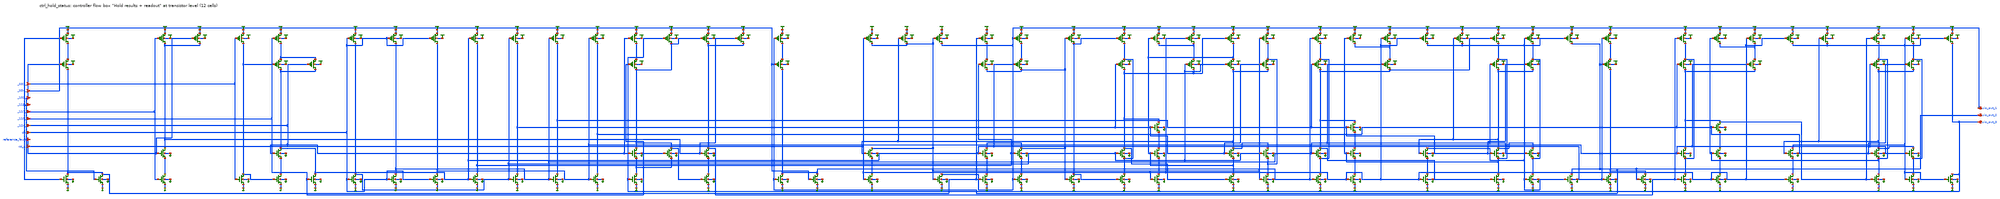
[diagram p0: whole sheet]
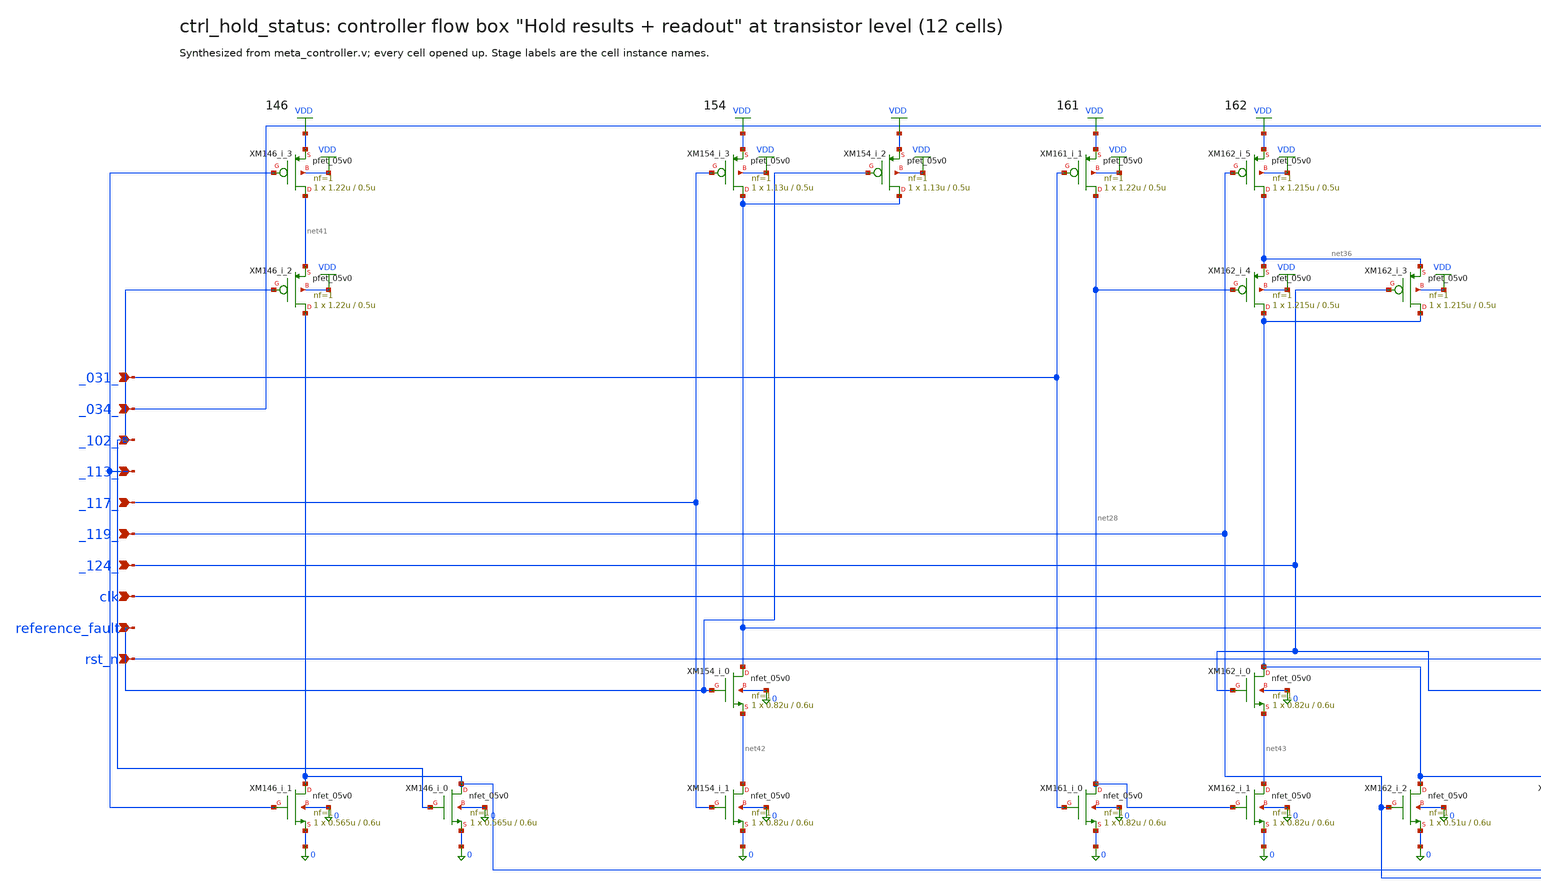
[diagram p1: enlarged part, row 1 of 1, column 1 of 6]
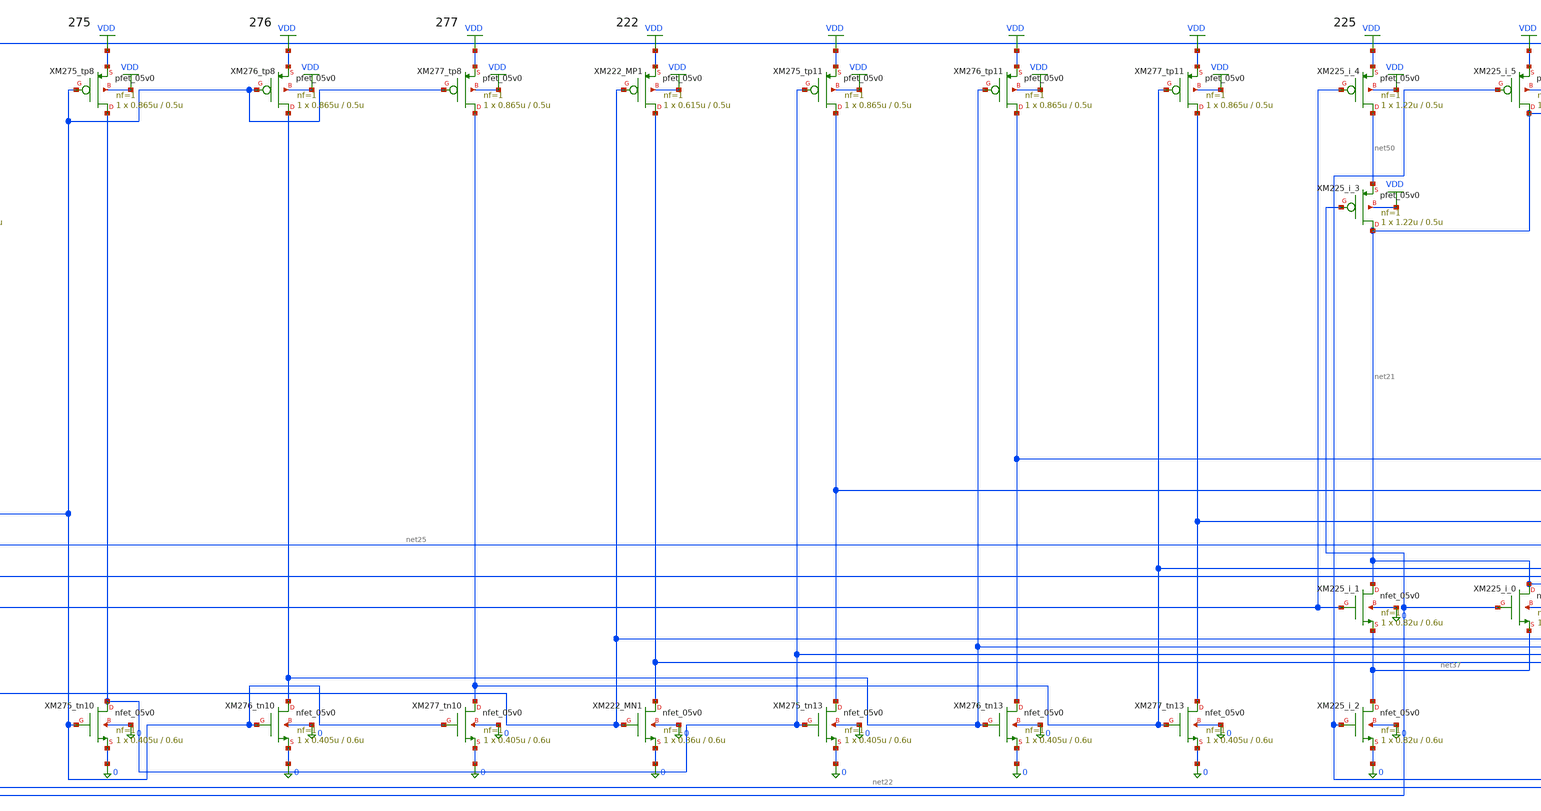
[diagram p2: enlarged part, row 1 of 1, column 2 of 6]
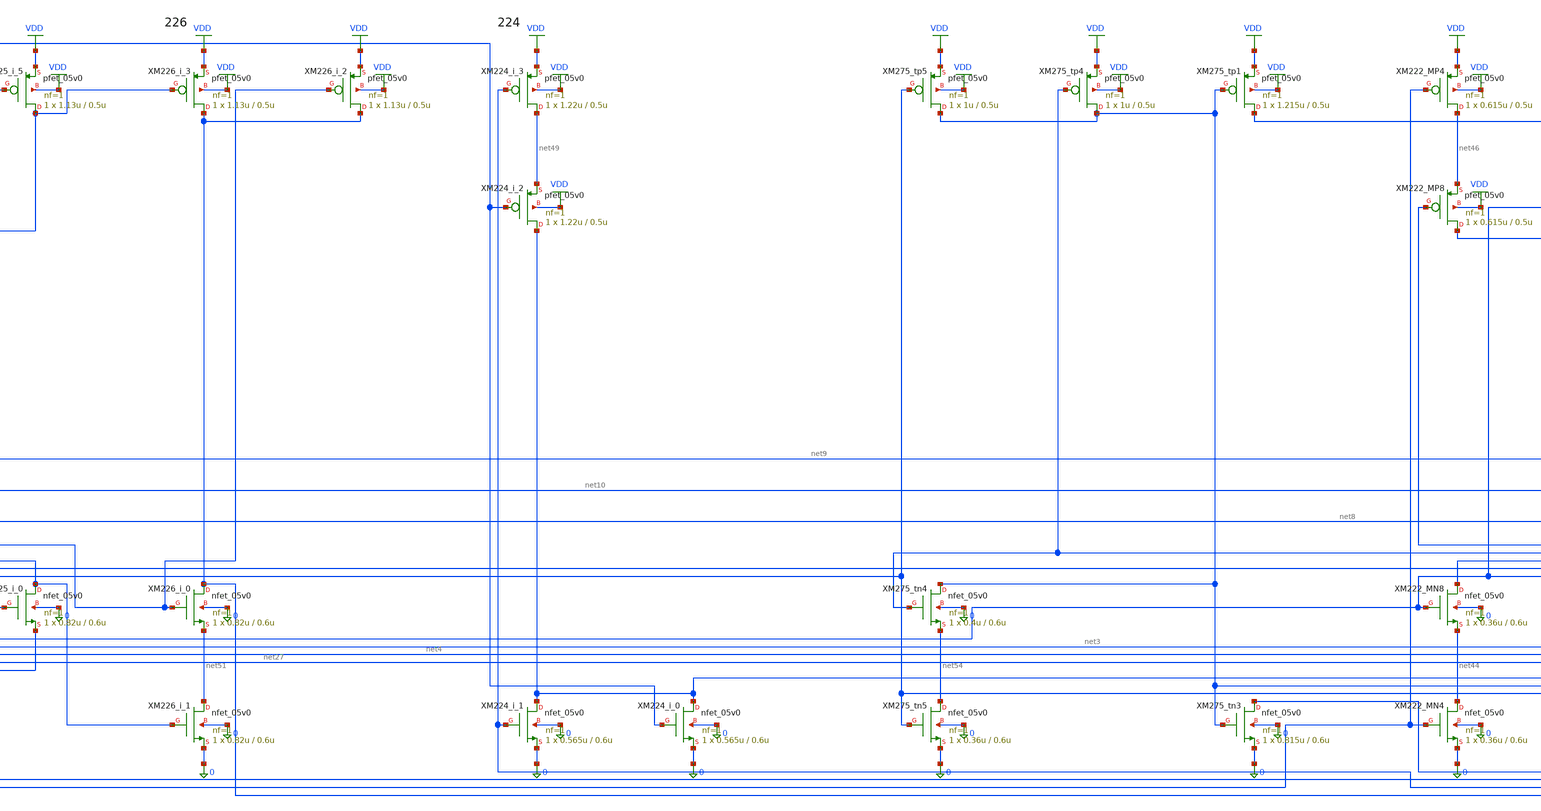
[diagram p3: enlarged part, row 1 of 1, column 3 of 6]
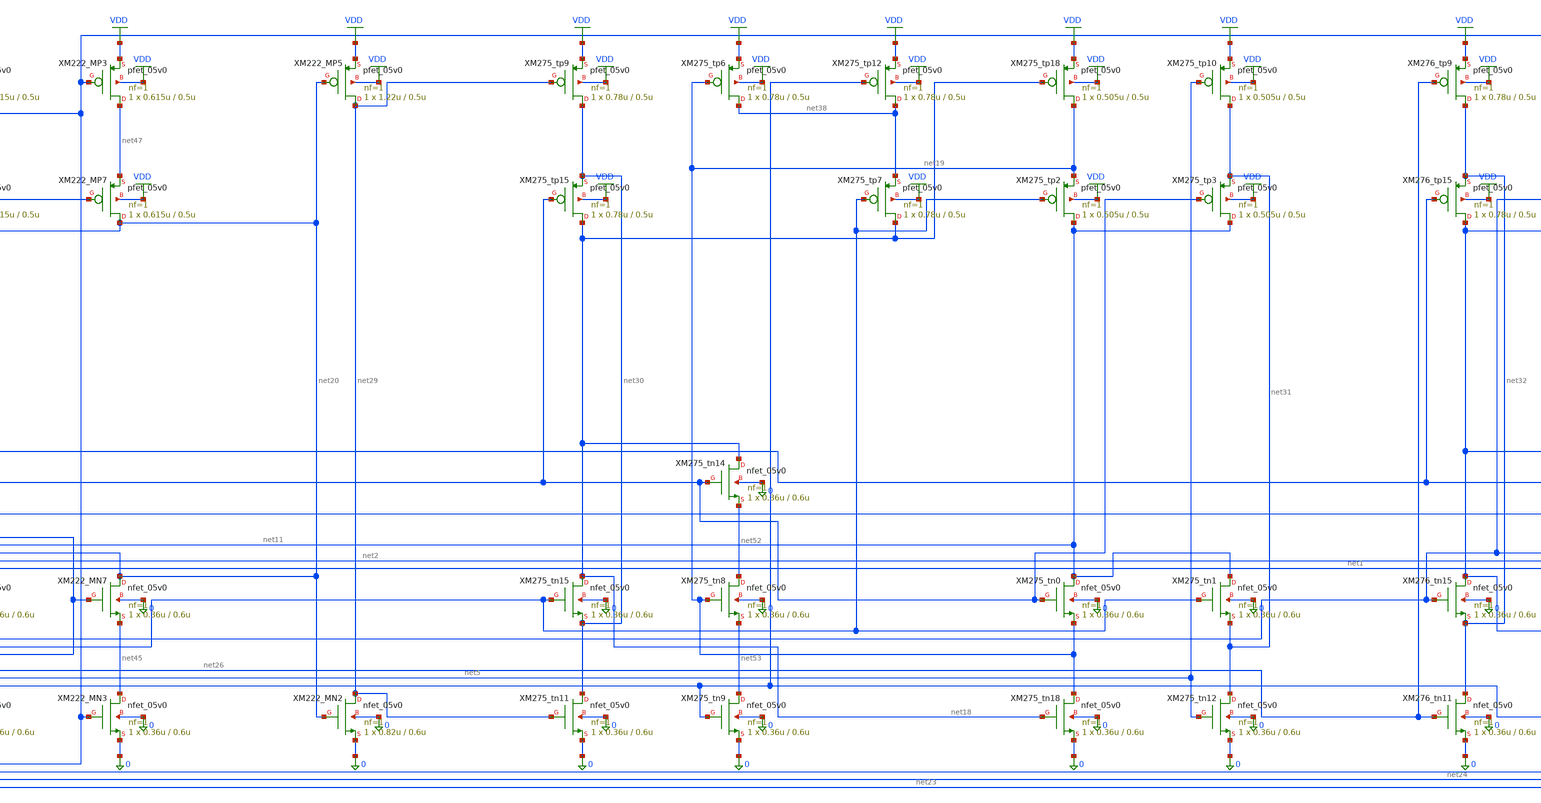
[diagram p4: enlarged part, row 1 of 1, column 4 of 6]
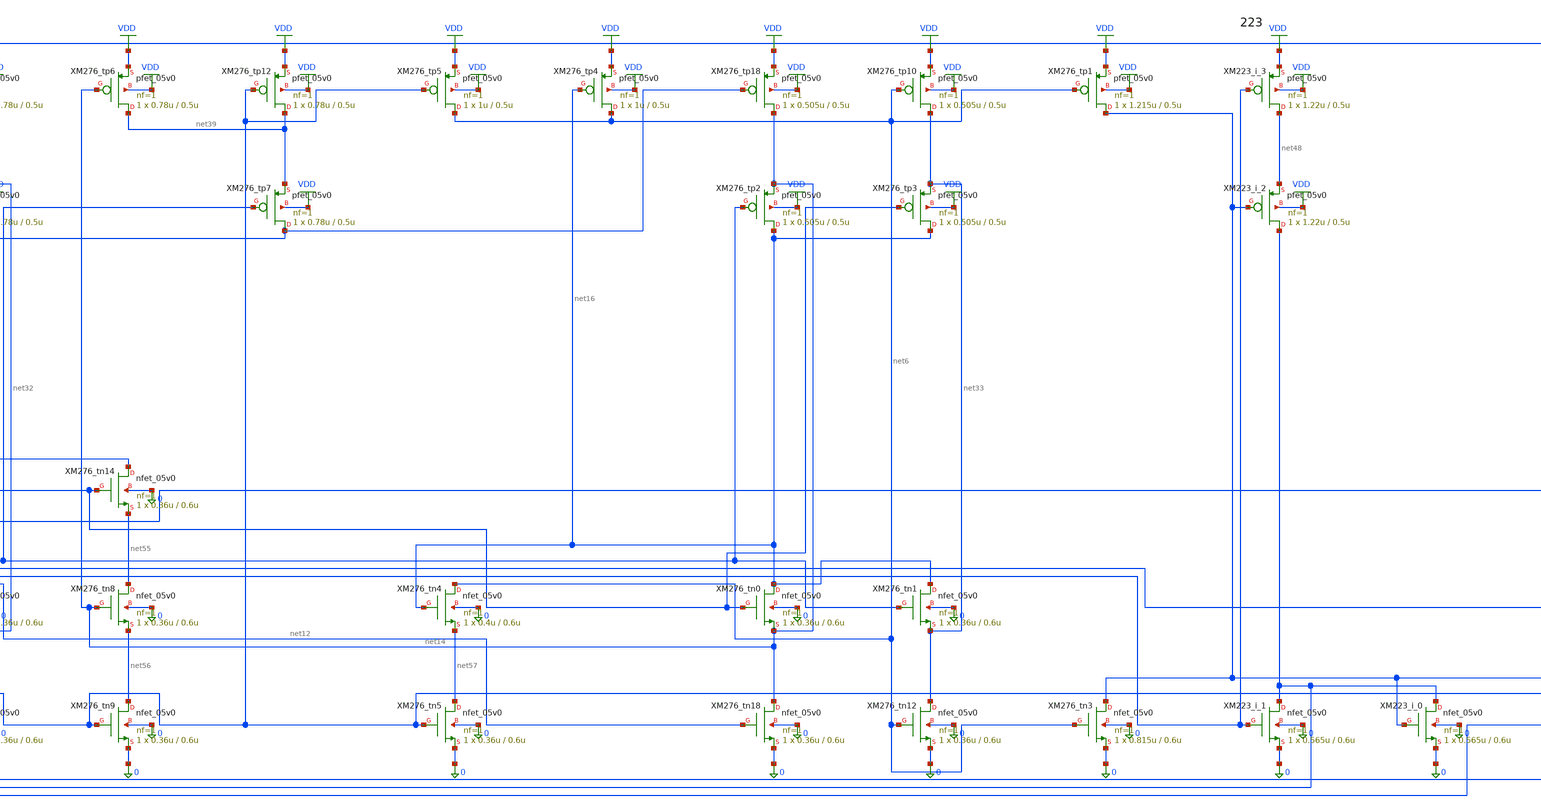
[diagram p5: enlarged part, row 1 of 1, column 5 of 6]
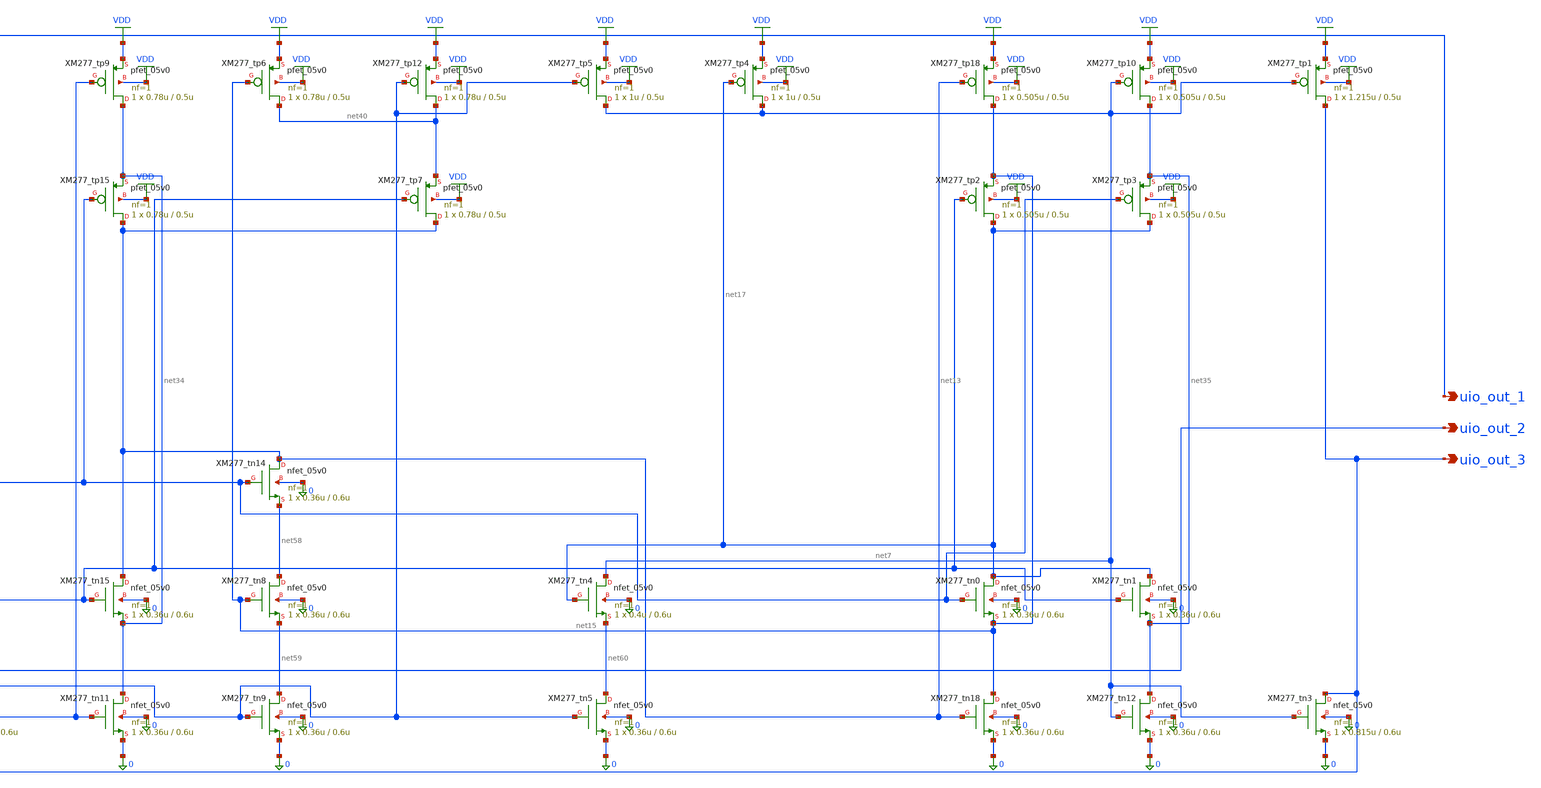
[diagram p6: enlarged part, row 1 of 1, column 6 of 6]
** sch_path: xschem/flat/ctrl_hold_status.sch
**.subckt ctrl_hold_status _031_ _034_ _102_ _113_ _117_ _119_ _124_ clk reference_fault rst_n
*+ uio_out_1 uio_out_2 uio_out_3
*.ipin _031_
*.ipin _034_
*.ipin _102_
*.ipin _113_
*.ipin _117_
*.ipin _119_
*.ipin _124_
*.ipin clk
*.ipin reference_fault
*.ipin rst_n
*.opin uio_out_1
*.opin uio_out_2
*.opin uio_out_3
XM146_i_1 net22 _113_ 0 0 nfet_05v0 L=0.6u W=0.565u nf=1 ad=2.825e-13 as=2.825e-13 pd=2.13e-06
+ ps=2.13e-06 nrd=0 nrs=0 sa=0 sb=0 sd=0 m=1
XM146_i_0 net22 _102_ 0 0 nfet_05v0 L=0.6u W=0.565u nf=1 ad=2.825e-13 as=2.825e-13 pd=2.13e-06
+ ps=2.13e-06 nrd=0 nrs=0 sa=0 sb=0 sd=0 m=1
XM146_i_3 net41 _113_ VDD VDD pfet_05v0 L=0.5u W=1.22u nf=1 ad=6.1e-13 as=6.1e-13 pd=3.44e-06
+ ps=3.44e-06 nrd=0 nrs=0 sa=0 sb=0 sd=0 m=1
XM146_i_2 net22 _102_ net41 VDD pfet_05v0 L=0.5u W=1.22u nf=1 ad=6.1e-13 as=6.1e-13 pd=3.44e-06
+ ps=3.44e-06 nrd=0 nrs=0 sa=0 sb=0 sd=0 m=1
XM154_i_1 net42 _117_ 0 0 nfet_05v0 L=0.6u W=0.82u nf=1 ad=4.1e-13 as=4.1e-13 pd=2.64e-06
+ ps=2.64e-06 nrd=0 nrs=0 sa=0 sb=0 sd=0 m=1
XM154_i_0 net25 reference_fault net42 0 nfet_05v0 L=0.6u W=0.82u nf=1 ad=4.1e-13 as=4.1e-13
+ pd=2.64e-06 ps=2.64e-06 nrd=0 nrs=0 sa=0 sb=0 sd=0 m=1
XM154_i_3 net25 _117_ VDD VDD pfet_05v0 L=0.5u W=1.13u nf=1 ad=5.65e-13 as=5.65e-13 pd=3.26e-06
+ ps=3.26e-06 nrd=0 nrs=0 sa=0 sb=0 sd=0 m=1
XM154_i_2 net25 reference_fault VDD VDD pfet_05v0 L=0.5u W=1.13u nf=1 ad=5.65e-13 as=5.65e-13
+ pd=3.26e-06 ps=3.26e-06 nrd=0 nrs=0 sa=0 sb=0 sd=0 m=1
XM161_i_0 net28 _031_ 0 0 nfet_05v0 L=0.6u W=0.82u nf=1 ad=4.1e-13 as=4.1e-13 pd=2.64e-06
+ ps=2.64e-06 nrd=0 nrs=0 sa=0 sb=0 sd=0 m=1
XM161_i_1 net28 _031_ VDD VDD pfet_05v0 L=0.5u W=1.22u nf=1 ad=6.1e-13 as=6.1e-13 pd=3.44e-06
+ ps=3.44e-06 nrd=0 nrs=0 sa=0 sb=0 sd=0 m=1
XM162_i_1 net43 net28 0 0 nfet_05v0 L=0.6u W=0.82u nf=1 ad=4.1e-13 as=4.1e-13 pd=2.64e-06
+ ps=2.64e-06 nrd=0 nrs=0 sa=0 sb=0 sd=0 m=1
XM162_i_0 net1 _124_ net43 0 nfet_05v0 L=0.6u W=0.82u nf=1 ad=4.1e-13 as=4.1e-13 pd=2.64e-06
+ ps=2.64e-06 nrd=0 nrs=0 sa=0 sb=0 sd=0 m=1
XM162_i_2 net1 _119_ 0 0 nfet_05v0 L=0.6u W=0.51u nf=1 ad=2.55e-13 as=2.55e-13 pd=2.02e-06
+ ps=2.02e-06 nrd=0 nrs=0 sa=0 sb=0 sd=0 m=1
XM162_i_4 net1 net28 net36 VDD pfet_05v0 L=0.5u W=1.215u nf=1 ad=6.075e-13 as=6.075e-13 pd=3.43e-06
+ ps=3.43e-06 nrd=0 nrs=0 sa=0 sb=0 sd=0 m=1
XM162_i_3 net1 _124_ net36 VDD pfet_05v0 L=0.5u W=1.215u nf=1 ad=6.075e-13 as=6.075e-13 pd=3.43e-06
+ ps=3.43e-06 nrd=0 nrs=0 sa=0 sb=0 sd=0 m=1
XM162_i_5 net36 _119_ VDD VDD pfet_05v0 L=0.5u W=1.215u nf=1 ad=6.075e-13 as=6.075e-13 pd=3.43e-06
+ ps=3.43e-06 nrd=0 nrs=0 sa=0 sb=0 sd=0 m=1
XM222_MN2 net29 net20 0 0 nfet_05v0 L=0.6u W=0.82u nf=1 ad=4.1e-13 as=4.1e-13 pd=2.64e-06
+ ps=2.64e-06 nrd=0 nrs=0 sa=0 sb=0 sd=0 m=1
XM222_MN4 net44 net22 0 0 nfet_05v0 L=0.6u W=0.36u nf=1 ad=1.8e-13 as=1.8e-13 pd=1.72e-06
+ ps=1.72e-06 nrd=0 nrs=0 sa=0 sb=0 sd=0 m=1
XM222_MN8 net20 net1 net44 0 nfet_05v0 L=0.6u W=0.36u nf=1 ad=1.8e-13 as=1.8e-13 pd=1.72e-06
+ ps=1.72e-06 nrd=0 nrs=0 sa=0 sb=0 sd=0 m=1
XM222_MN7 net20 net27 net45 0 nfet_05v0 L=0.6u W=0.36u nf=1 ad=1.8e-13 as=1.8e-13 pd=1.72e-06
+ ps=1.72e-06 nrd=0 nrs=0 sa=0 sb=0 sd=0 m=1
XM222_MN3 net45 uio_out_1 0 0 nfet_05v0 L=0.6u W=0.36u nf=1 ad=1.8e-13 as=1.8e-13 pd=1.72e-06
+ ps=1.72e-06 nrd=0 nrs=0 sa=0 sb=0 sd=0 m=1
XM222_MN1 net27 net1 0 0 nfet_05v0 L=0.6u W=0.36u nf=1 ad=1.8e-13 as=1.8e-13 pd=1.72e-06 ps=1.72e-06
+ nrd=0 nrs=0 sa=0 sb=0 sd=0 m=1
XM222_MP5 net29 net20 VDD VDD pfet_05v0 L=0.5u W=1.22u nf=1 ad=6.1e-13 as=6.1e-13 pd=3.44e-06
+ ps=3.44e-06 nrd=0 nrs=0 sa=0 sb=0 sd=0 m=1
XM222_MP4 net46 net22 VDD VDD pfet_05v0 L=0.5u W=0.615u nf=1 ad=3.075e-13 as=3.075e-13 pd=2.23e-06
+ ps=2.23e-06 nrd=0 nrs=0 sa=0 sb=0 sd=0 m=1
XM222_MP8 net20 net27 net46 VDD pfet_05v0 L=0.5u W=0.615u nf=1 ad=3.075e-13 as=3.075e-13 pd=2.23e-06
+ ps=2.23e-06 nrd=0 nrs=0 sa=0 sb=0 sd=0 m=1
XM222_MP7 net20 net1 net47 VDD pfet_05v0 L=0.5u W=0.615u nf=1 ad=3.075e-13 as=3.075e-13 pd=2.23e-06
+ ps=2.23e-06 nrd=0 nrs=0 sa=0 sb=0 sd=0 m=1
XM222_MP3 net47 uio_out_1 VDD VDD pfet_05v0 L=0.5u W=0.615u nf=1 ad=3.075e-13 as=3.075e-13
+ pd=2.23e-06 ps=2.23e-06 nrd=0 nrs=0 sa=0 sb=0 sd=0 m=1
XM222_MP1 net27 net1 VDD VDD pfet_05v0 L=0.5u W=0.615u nf=1 ad=3.075e-13 as=3.075e-13 pd=2.23e-06
+ ps=2.23e-06 nrd=0 nrs=0 sa=0 sb=0 sd=0 m=1
XM223_i_1 net24 net1 0 0 nfet_05v0 L=0.6u W=0.565u nf=1 ad=2.825e-13 as=2.825e-13 pd=2.13e-06
+ ps=2.13e-06 nrd=0 nrs=0 sa=0 sb=0 sd=0 m=1
XM223_i_0 net24 uio_out_2 0 0 nfet_05v0 L=0.6u W=0.565u nf=1 ad=2.825e-13 as=2.825e-13 pd=2.13e-06
+ ps=2.13e-06 nrd=0 nrs=0 sa=0 sb=0 sd=0 m=1
XM223_i_3 net48 net1 VDD VDD pfet_05v0 L=0.5u W=1.22u nf=1 ad=6.1e-13 as=6.1e-13 pd=3.44e-06
+ ps=3.44e-06 nrd=0 nrs=0 sa=0 sb=0 sd=0 m=1
XM223_i_2 net24 uio_out_2 net48 VDD pfet_05v0 L=0.5u W=1.22u nf=1 ad=6.1e-13 as=6.1e-13 pd=3.44e-06
+ ps=3.44e-06 nrd=0 nrs=0 sa=0 sb=0 sd=0 m=1
XM224_i_1 net26 net24 0 0 nfet_05v0 L=0.6u W=0.565u nf=1 ad=2.825e-13 as=2.825e-13 pd=2.13e-06
+ ps=2.13e-06 nrd=0 nrs=0 sa=0 sb=0 sd=0 m=1
XM224_i_0 net26 _034_ 0 0 nfet_05v0 L=0.6u W=0.565u nf=1 ad=2.825e-13 as=2.825e-13 pd=2.13e-06
+ ps=2.13e-06 nrd=0 nrs=0 sa=0 sb=0 sd=0 m=1
XM224_i_3 net49 net24 VDD VDD pfet_05v0 L=0.5u W=1.22u nf=1 ad=6.1e-13 as=6.1e-13 pd=3.44e-06
+ ps=3.44e-06 nrd=0 nrs=0 sa=0 sb=0 sd=0 m=1
XM224_i_2 net26 _034_ net49 VDD pfet_05v0 L=0.5u W=1.22u nf=1 ad=6.1e-13 as=6.1e-13 pd=3.44e-06
+ ps=3.44e-06 nrd=0 nrs=0 sa=0 sb=0 sd=0 m=1
XM225_i_1 net21 _124_ net37 0 nfet_05v0 L=0.6u W=0.82u nf=1 ad=4.1e-13 as=4.1e-13 pd=2.64e-06
+ ps=2.64e-06 nrd=0 nrs=0 sa=0 sb=0 sd=0 m=1
XM225_i_0 net21 _119_ net37 0 nfet_05v0 L=0.6u W=0.82u nf=1 ad=4.1e-13 as=4.1e-13 pd=2.64e-06
+ ps=2.64e-06 nrd=0 nrs=0 sa=0 sb=0 sd=0 m=1
XM225_i_2 net37 uio_out_3 0 0 nfet_05v0 L=0.6u W=0.82u nf=1 ad=4.1e-13 as=4.1e-13 pd=2.64e-06
+ ps=2.64e-06 nrd=0 nrs=0 sa=0 sb=0 sd=0 m=1
XM225_i_4 net50 _124_ VDD VDD pfet_05v0 L=0.5u W=1.22u nf=1 ad=6.1e-13 as=6.1e-13 pd=3.44e-06
+ ps=3.44e-06 nrd=0 nrs=0 sa=0 sb=0 sd=0 m=1
XM225_i_3 net21 _119_ net50 VDD pfet_05v0 L=0.5u W=1.22u nf=1 ad=6.1e-13 as=6.1e-13 pd=3.44e-06
+ ps=3.44e-06 nrd=0 nrs=0 sa=0 sb=0 sd=0 m=1
XM225_i_5 net21 uio_out_3 VDD VDD pfet_05v0 L=0.5u W=1.13u nf=1 ad=5.65e-13 as=5.65e-13 pd=3.26e-06
+ ps=3.26e-06 nrd=0 nrs=0 sa=0 sb=0 sd=0 m=1
XM226_i_1 net51 net21 0 0 nfet_05v0 L=0.6u W=0.82u nf=1 ad=4.1e-13 as=4.1e-13 pd=2.64e-06
+ ps=2.64e-06 nrd=0 nrs=0 sa=0 sb=0 sd=0 m=1
XM226_i_0 net23 net25 net51 0 nfet_05v0 L=0.6u W=0.82u nf=1 ad=4.1e-13 as=4.1e-13 pd=2.64e-06
+ ps=2.64e-06 nrd=0 nrs=0 sa=0 sb=0 sd=0 m=1
XM226_i_3 net23 net21 VDD VDD pfet_05v0 L=0.5u W=1.13u nf=1 ad=5.65e-13 as=5.65e-13 pd=3.26e-06
+ ps=3.26e-06 nrd=0 nrs=0 sa=0 sb=0 sd=0 m=1
XM226_i_2 net23 net25 VDD VDD pfet_05v0 L=0.5u W=1.13u nf=1 ad=5.65e-13 as=5.65e-13 pd=3.26e-06
+ ps=3.26e-06 nrd=0 nrs=0 sa=0 sb=0 sd=0 m=1
XM275_tn10 net4 clk 0 0 nfet_05v0 L=0.6u W=0.405u nf=1 ad=2.025e-13 as=2.025e-13 pd=1.81e-06
+ ps=1.81e-06 nrd=0 nrs=0 sa=0 sb=0 sd=0 m=1
XM275_tn13 net10 net4 0 0 nfet_05v0 L=0.6u W=0.405u nf=1 ad=2.025e-13 as=2.025e-13 pd=1.81e-06
+ ps=1.81e-06 nrd=0 nrs=0 sa=0 sb=0 sd=0 m=1
XM275_tn11 net30 net29 0 0 nfet_05v0 L=0.6u W=0.36u nf=1 ad=1.8e-13 as=1.8e-13 pd=1.72e-06
+ ps=1.72e-06 nrd=0 nrs=0 sa=0 sb=0 sd=0 m=1
XM275_tn15 net18 net4 net30 0 nfet_05v0 L=0.6u W=0.36u nf=1 ad=1.8e-13 as=1.8e-13 pd=1.72e-06
+ ps=1.72e-06 nrd=0 nrs=0 sa=0 sb=0 sd=0 m=1
XM275_tn14 net18 net10 net52 0 nfet_05v0 L=0.6u W=0.36u nf=1 ad=1.8e-13 as=1.8e-13 pd=1.72e-06
+ ps=1.72e-06 nrd=0 nrs=0 sa=0 sb=0 sd=0 m=1
XM275_tn8 net52 net19 net53 0 nfet_05v0 L=0.6u W=0.36u nf=1 ad=1.8e-13 as=1.8e-13 pd=1.72e-06
+ ps=1.72e-06 nrd=0 nrs=0 sa=0 sb=0 sd=0 m=1
XM275_tn9 net53 rst_n 0 0 nfet_05v0 L=0.6u W=0.36u nf=1 ad=1.8e-13 as=1.8e-13 pd=1.72e-06
+ ps=1.72e-06 nrd=0 nrs=0 sa=0 sb=0 sd=0 m=1
XM275_tn18 net19 net18 0 0 nfet_05v0 L=0.6u W=0.36u nf=1 ad=1.8e-13 as=1.8e-13 pd=1.72e-06
+ ps=1.72e-06 nrd=0 nrs=0 sa=0 sb=0 sd=0 m=1
XM275_tn0 net11 net10 net19 0 nfet_05v0 L=0.6u W=0.36u nf=1 ad=1.8e-13 as=1.8e-13 pd=1.72e-06
+ ps=1.72e-06 nrd=0 nrs=0 sa=0 sb=0 sd=0 m=1
XM275_tn1 net11 net4 net31 0 nfet_05v0 L=0.6u W=0.36u nf=1 ad=1.8e-13 as=1.8e-13 pd=1.72e-06
+ ps=1.72e-06 nrd=0 nrs=0 sa=0 sb=0 sd=0 m=1
XM275_tn12 net31 net5 0 0 nfet_05v0 L=0.6u W=0.36u nf=1 ad=1.8e-13 as=1.8e-13 pd=1.72e-06
+ ps=1.72e-06 nrd=0 nrs=0 sa=0 sb=0 sd=0 m=1
XM275_tn5 net54 rst_n 0 0 nfet_05v0 L=0.6u W=0.36u nf=1 ad=1.8e-13 as=1.8e-13 pd=1.72e-06
+ ps=1.72e-06 nrd=0 nrs=0 sa=0 sb=0 sd=0 m=1
XM275_tn4 net5 net11 net54 0 nfet_05v0 L=0.6u W=0.4u nf=1 ad=2e-13 as=2e-13 pd=1.8e-06 ps=1.8e-06
+ nrd=0 nrs=0 sa=0 sb=0 sd=0 m=1
XM275_tn3 uio_out_1 net5 0 0 nfet_05v0 L=0.6u W=0.815u nf=1 ad=4.075e-13 as=4.075e-13 pd=2.63e-06
+ ps=2.63e-06 nrd=0 nrs=0 sa=0 sb=0 sd=0 m=1
XM275_tp8 net4 clk VDD VDD pfet_05v0 L=0.5u W=0.865u nf=1 ad=4.325e-13 as=4.325e-13 pd=2.73e-06
+ ps=2.73e-06 nrd=0 nrs=0 sa=0 sb=0 sd=0 m=1
XM275_tp11 net10 net4 VDD VDD pfet_05v0 L=0.5u W=0.865u nf=1 ad=4.325e-13 as=4.325e-13 pd=2.73e-06
+ ps=2.73e-06 nrd=0 nrs=0 sa=0 sb=0 sd=0 m=1
XM275_tp9 net30 net29 VDD VDD pfet_05v0 L=0.5u W=0.78u nf=1 ad=3.9e-13 as=3.9e-13 pd=2.56e-06
+ ps=2.56e-06 nrd=0 nrs=0 sa=0 sb=0 sd=0 m=1
XM275_tp15 net18 net10 net30 VDD pfet_05v0 L=0.5u W=0.78u nf=1 ad=3.9e-13 as=3.9e-13 pd=2.56e-06
+ ps=2.56e-06 nrd=0 nrs=0 sa=0 sb=0 sd=0 m=1
XM275_tp7 net18 net4 net38 VDD pfet_05v0 L=0.5u W=0.78u nf=1 ad=3.9e-13 as=3.9e-13 pd=2.56e-06
+ ps=2.56e-06 nrd=0 nrs=0 sa=0 sb=0 sd=0 m=1
XM275_tp6 net38 net19 VDD VDD pfet_05v0 L=0.5u W=0.78u nf=1 ad=3.9e-13 as=3.9e-13 pd=2.56e-06
+ ps=2.56e-06 nrd=0 nrs=0 sa=0 sb=0 sd=0 m=1
XM275_tp12 net38 rst_n VDD VDD pfet_05v0 L=0.5u W=0.78u nf=1 ad=3.9e-13 as=3.9e-13 pd=2.56e-06
+ ps=2.56e-06 nrd=0 nrs=0 sa=0 sb=0 sd=0 m=1
XM275_tp18 net19 net18 VDD VDD pfet_05v0 L=0.5u W=0.505u nf=1 ad=2.525e-13 as=2.525e-13 pd=2.01e-06
+ ps=2.01e-06 nrd=0 nrs=0 sa=0 sb=0 sd=0 m=1
XM275_tp2 net11 net4 net19 VDD pfet_05v0 L=0.5u W=0.505u nf=1 ad=2.525e-13 as=2.525e-13 pd=2.01e-06
+ ps=2.01e-06 nrd=0 nrs=0 sa=0 sb=0 sd=0 m=1
XM275_tp3 net11 net10 net31 VDD pfet_05v0 L=0.5u W=0.505u nf=1 ad=2.525e-13 as=2.525e-13 pd=2.01e-06
+ ps=2.01e-06 nrd=0 nrs=0 sa=0 sb=0 sd=0 m=1
XM275_tp10 net31 net5 VDD VDD pfet_05v0 L=0.5u W=0.505u nf=1 ad=2.525e-13 as=2.525e-13 pd=2.01e-06
+ ps=2.01e-06 nrd=0 nrs=0 sa=0 sb=0 sd=0 m=1
XM275_tp5 net5 rst_n VDD VDD pfet_05v0 L=0.5u W=1u nf=1 ad=5e-13 as=5e-13 pd=3e-06 ps=3e-06 nrd=0
+ nrs=0 sa=0 sb=0 sd=0 m=1
XM275_tp4 net5 net11 VDD VDD pfet_05v0 L=0.5u W=1u nf=1 ad=5e-13 as=5e-13 pd=3e-06 ps=3e-06 nrd=0
+ nrs=0 sa=0 sb=0 sd=0 m=1
XM275_tp1 uio_out_1 net5 VDD VDD pfet_05v0 L=0.5u W=1.215u nf=1 ad=6.075e-13 as=6.075e-13
+ pd=3.43e-06 ps=3.43e-06 nrd=0 nrs=0 sa=0 sb=0 sd=0 m=1
XM276_tn10 net3 clk 0 0 nfet_05v0 L=0.6u W=0.405u nf=1 ad=2.025e-13 as=2.025e-13 pd=1.81e-06
+ ps=1.81e-06 nrd=0 nrs=0 sa=0 sb=0 sd=0 m=1
XM276_tn13 net9 net3 0 0 nfet_05v0 L=0.6u W=0.405u nf=1 ad=2.025e-13 as=2.025e-13 pd=1.81e-06
+ ps=1.81e-06 nrd=0 nrs=0 sa=0 sb=0 sd=0 m=1
XM276_tn11 net32 net26 0 0 nfet_05v0 L=0.6u W=0.36u nf=1 ad=1.8e-13 as=1.8e-13 pd=1.72e-06
+ ps=1.72e-06 nrd=0 nrs=0 sa=0 sb=0 sd=0 m=1
XM276_tn15 net12 net3 net32 0 nfet_05v0 L=0.6u W=0.36u nf=1 ad=1.8e-13 as=1.8e-13 pd=1.72e-06
+ ps=1.72e-06 nrd=0 nrs=0 sa=0 sb=0 sd=0 m=1
XM276_tn14 net12 net9 net55 0 nfet_05v0 L=0.6u W=0.36u nf=1 ad=1.8e-13 as=1.8e-13 pd=1.72e-06
+ ps=1.72e-06 nrd=0 nrs=0 sa=0 sb=0 sd=0 m=1
XM276_tn8 net55 net14 net56 0 nfet_05v0 L=0.6u W=0.36u nf=1 ad=1.8e-13 as=1.8e-13 pd=1.72e-06
+ ps=1.72e-06 nrd=0 nrs=0 sa=0 sb=0 sd=0 m=1
XM276_tn9 net56 rst_n 0 0 nfet_05v0 L=0.6u W=0.36u nf=1 ad=1.8e-13 as=1.8e-13 pd=1.72e-06
+ ps=1.72e-06 nrd=0 nrs=0 sa=0 sb=0 sd=0 m=1
XM276_tn18 net14 net12 0 0 nfet_05v0 L=0.6u W=0.36u nf=1 ad=1.8e-13 as=1.8e-13 pd=1.72e-06
+ ps=1.72e-06 nrd=0 nrs=0 sa=0 sb=0 sd=0 m=1
XM276_tn0 net16 net9 net14 0 nfet_05v0 L=0.6u W=0.36u nf=1 ad=1.8e-13 as=1.8e-13 pd=1.72e-06
+ ps=1.72e-06 nrd=0 nrs=0 sa=0 sb=0 sd=0 m=1
XM276_tn1 net16 net3 net33 0 nfet_05v0 L=0.6u W=0.36u nf=1 ad=1.8e-13 as=1.8e-13 pd=1.72e-06
+ ps=1.72e-06 nrd=0 nrs=0 sa=0 sb=0 sd=0 m=1
XM276_tn12 net33 net6 0 0 nfet_05v0 L=0.6u W=0.36u nf=1 ad=1.8e-13 as=1.8e-13 pd=1.72e-06
+ ps=1.72e-06 nrd=0 nrs=0 sa=0 sb=0 sd=0 m=1
XM276_tn5 net57 rst_n 0 0 nfet_05v0 L=0.6u W=0.36u nf=1 ad=1.8e-13 as=1.8e-13 pd=1.72e-06
+ ps=1.72e-06 nrd=0 nrs=0 sa=0 sb=0 sd=0 m=1
XM276_tn4 net6 net16 net57 0 nfet_05v0 L=0.6u W=0.4u nf=1 ad=2e-13 as=2e-13 pd=1.8e-06 ps=1.8e-06
+ nrd=0 nrs=0 sa=0 sb=0 sd=0 m=1
XM276_tn3 uio_out_2 net6 0 0 nfet_05v0 L=0.6u W=0.815u nf=1 ad=4.075e-13 as=4.075e-13 pd=2.63e-06
+ ps=2.63e-06 nrd=0 nrs=0 sa=0 sb=0 sd=0 m=1
XM276_tp8 net3 clk VDD VDD pfet_05v0 L=0.5u W=0.865u nf=1 ad=4.325e-13 as=4.325e-13 pd=2.73e-06
+ ps=2.73e-06 nrd=0 nrs=0 sa=0 sb=0 sd=0 m=1
XM276_tp11 net9 net3 VDD VDD pfet_05v0 L=0.5u W=0.865u nf=1 ad=4.325e-13 as=4.325e-13 pd=2.73e-06
+ ps=2.73e-06 nrd=0 nrs=0 sa=0 sb=0 sd=0 m=1
XM276_tp9 net32 net26 VDD VDD pfet_05v0 L=0.5u W=0.78u nf=1 ad=3.9e-13 as=3.9e-13 pd=2.56e-06
+ ps=2.56e-06 nrd=0 nrs=0 sa=0 sb=0 sd=0 m=1
XM276_tp15 net12 net9 net32 VDD pfet_05v0 L=0.5u W=0.78u nf=1 ad=3.9e-13 as=3.9e-13 pd=2.56e-06
+ ps=2.56e-06 nrd=0 nrs=0 sa=0 sb=0 sd=0 m=1
XM276_tp7 net12 net3 net39 VDD pfet_05v0 L=0.5u W=0.78u nf=1 ad=3.9e-13 as=3.9e-13 pd=2.56e-06
+ ps=2.56e-06 nrd=0 nrs=0 sa=0 sb=0 sd=0 m=1
XM276_tp6 net39 net14 VDD VDD pfet_05v0 L=0.5u W=0.78u nf=1 ad=3.9e-13 as=3.9e-13 pd=2.56e-06
+ ps=2.56e-06 nrd=0 nrs=0 sa=0 sb=0 sd=0 m=1
XM276_tp12 net39 rst_n VDD VDD pfet_05v0 L=0.5u W=0.78u nf=1 ad=3.9e-13 as=3.9e-13 pd=2.56e-06
+ ps=2.56e-06 nrd=0 nrs=0 sa=0 sb=0 sd=0 m=1
XM276_tp18 net14 net12 VDD VDD pfet_05v0 L=0.5u W=0.505u nf=1 ad=2.525e-13 as=2.525e-13 pd=2.01e-06
+ ps=2.01e-06 nrd=0 nrs=0 sa=0 sb=0 sd=0 m=1
XM276_tp2 net16 net3 net14 VDD pfet_05v0 L=0.5u W=0.505u nf=1 ad=2.525e-13 as=2.525e-13 pd=2.01e-06
+ ps=2.01e-06 nrd=0 nrs=0 sa=0 sb=0 sd=0 m=1
XM276_tp3 net16 net9 net33 VDD pfet_05v0 L=0.5u W=0.505u nf=1 ad=2.525e-13 as=2.525e-13 pd=2.01e-06
+ ps=2.01e-06 nrd=0 nrs=0 sa=0 sb=0 sd=0 m=1
XM276_tp10 net33 net6 VDD VDD pfet_05v0 L=0.5u W=0.505u nf=1 ad=2.525e-13 as=2.525e-13 pd=2.01e-06
+ ps=2.01e-06 nrd=0 nrs=0 sa=0 sb=0 sd=0 m=1
XM276_tp5 net6 rst_n VDD VDD pfet_05v0 L=0.5u W=1u nf=1 ad=5e-13 as=5e-13 pd=3e-06 ps=3e-06 nrd=0
+ nrs=0 sa=0 sb=0 sd=0 m=1
XM276_tp4 net6 net16 VDD VDD pfet_05v0 L=0.5u W=1u nf=1 ad=5e-13 as=5e-13 pd=3e-06 ps=3e-06 nrd=0
+ nrs=0 sa=0 sb=0 sd=0 m=1
XM276_tp1 uio_out_2 net6 VDD VDD pfet_05v0 L=0.5u W=1.215u nf=1 ad=6.075e-13 as=6.075e-13
+ pd=3.43e-06 ps=3.43e-06 nrd=0 nrs=0 sa=0 sb=0 sd=0 m=1
XM277_tn10 net2 clk 0 0 nfet_05v0 L=0.6u W=0.405u nf=1 ad=2.025e-13 as=2.025e-13 pd=1.81e-06
+ ps=1.81e-06 nrd=0 nrs=0 sa=0 sb=0 sd=0 m=1
XM277_tn13 net8 net2 0 0 nfet_05v0 L=0.6u W=0.405u nf=1 ad=2.025e-13 as=2.025e-13 pd=1.81e-06
+ ps=1.81e-06 nrd=0 nrs=0 sa=0 sb=0 sd=0 m=1
XM277_tn11 net34 net23 0 0 nfet_05v0 L=0.6u W=0.36u nf=1 ad=1.8e-13 as=1.8e-13 pd=1.72e-06
+ ps=1.72e-06 nrd=0 nrs=0 sa=0 sb=0 sd=0 m=1
XM277_tn15 net13 net2 net34 0 nfet_05v0 L=0.6u W=0.36u nf=1 ad=1.8e-13 as=1.8e-13 pd=1.72e-06
+ ps=1.72e-06 nrd=0 nrs=0 sa=0 sb=0 sd=0 m=1
XM277_tn14 net13 net8 net58 0 nfet_05v0 L=0.6u W=0.36u nf=1 ad=1.8e-13 as=1.8e-13 pd=1.72e-06
+ ps=1.72e-06 nrd=0 nrs=0 sa=0 sb=0 sd=0 m=1
XM277_tn8 net58 net15 net59 0 nfet_05v0 L=0.6u W=0.36u nf=1 ad=1.8e-13 as=1.8e-13 pd=1.72e-06
+ ps=1.72e-06 nrd=0 nrs=0 sa=0 sb=0 sd=0 m=1
XM277_tn9 net59 rst_n 0 0 nfet_05v0 L=0.6u W=0.36u nf=1 ad=1.8e-13 as=1.8e-13 pd=1.72e-06
+ ps=1.72e-06 nrd=0 nrs=0 sa=0 sb=0 sd=0 m=1
XM277_tn18 net15 net13 0 0 nfet_05v0 L=0.6u W=0.36u nf=1 ad=1.8e-13 as=1.8e-13 pd=1.72e-06
+ ps=1.72e-06 nrd=0 nrs=0 sa=0 sb=0 sd=0 m=1
XM277_tn0 net17 net8 net15 0 nfet_05v0 L=0.6u W=0.36u nf=1 ad=1.8e-13 as=1.8e-13 pd=1.72e-06
+ ps=1.72e-06 nrd=0 nrs=0 sa=0 sb=0 sd=0 m=1
XM277_tn1 net17 net2 net35 0 nfet_05v0 L=0.6u W=0.36u nf=1 ad=1.8e-13 as=1.8e-13 pd=1.72e-06
+ ps=1.72e-06 nrd=0 nrs=0 sa=0 sb=0 sd=0 m=1
XM277_tn12 net35 net7 0 0 nfet_05v0 L=0.6u W=0.36u nf=1 ad=1.8e-13 as=1.8e-13 pd=1.72e-06
+ ps=1.72e-06 nrd=0 nrs=0 sa=0 sb=0 sd=0 m=1
XM277_tn5 net60 rst_n 0 0 nfet_05v0 L=0.6u W=0.36u nf=1 ad=1.8e-13 as=1.8e-13 pd=1.72e-06
+ ps=1.72e-06 nrd=0 nrs=0 sa=0 sb=0 sd=0 m=1
XM277_tn4 net7 net17 net60 0 nfet_05v0 L=0.6u W=0.4u nf=1 ad=2e-13 as=2e-13 pd=1.8e-06 ps=1.8e-06
+ nrd=0 nrs=0 sa=0 sb=0 sd=0 m=1
XM277_tn3 uio_out_3 net7 0 0 nfet_05v0 L=0.6u W=0.815u nf=1 ad=4.075e-13 as=4.075e-13 pd=2.63e-06
+ ps=2.63e-06 nrd=0 nrs=0 sa=0 sb=0 sd=0 m=1
XM277_tp8 net2 clk VDD VDD pfet_05v0 L=0.5u W=0.865u nf=1 ad=4.325e-13 as=4.325e-13 pd=2.73e-06
+ ps=2.73e-06 nrd=0 nrs=0 sa=0 sb=0 sd=0 m=1
XM277_tp11 net8 net2 VDD VDD pfet_05v0 L=0.5u W=0.865u nf=1 ad=4.325e-13 as=4.325e-13 pd=2.73e-06
+ ps=2.73e-06 nrd=0 nrs=0 sa=0 sb=0 sd=0 m=1
XM277_tp9 net34 net23 VDD VDD pfet_05v0 L=0.5u W=0.78u nf=1 ad=3.9e-13 as=3.9e-13 pd=2.56e-06
+ ps=2.56e-06 nrd=0 nrs=0 sa=0 sb=0 sd=0 m=1
XM277_tp15 net13 net8 net34 VDD pfet_05v0 L=0.5u W=0.78u nf=1 ad=3.9e-13 as=3.9e-13 pd=2.56e-06
+ ps=2.56e-06 nrd=0 nrs=0 sa=0 sb=0 sd=0 m=1
XM277_tp7 net13 net2 net40 VDD pfet_05v0 L=0.5u W=0.78u nf=1 ad=3.9e-13 as=3.9e-13 pd=2.56e-06
+ ps=2.56e-06 nrd=0 nrs=0 sa=0 sb=0 sd=0 m=1
XM277_tp6 net40 net15 VDD VDD pfet_05v0 L=0.5u W=0.78u nf=1 ad=3.9e-13 as=3.9e-13 pd=2.56e-06
+ ps=2.56e-06 nrd=0 nrs=0 sa=0 sb=0 sd=0 m=1
XM277_tp12 net40 rst_n VDD VDD pfet_05v0 L=0.5u W=0.78u nf=1 ad=3.9e-13 as=3.9e-13 pd=2.56e-06
+ ps=2.56e-06 nrd=0 nrs=0 sa=0 sb=0 sd=0 m=1
XM277_tp18 net15 net13 VDD VDD pfet_05v0 L=0.5u W=0.505u nf=1 ad=2.525e-13 as=2.525e-13 pd=2.01e-06
+ ps=2.01e-06 nrd=0 nrs=0 sa=0 sb=0 sd=0 m=1
XM277_tp2 net17 net2 net15 VDD pfet_05v0 L=0.5u W=0.505u nf=1 ad=2.525e-13 as=2.525e-13 pd=2.01e-06
+ ps=2.01e-06 nrd=0 nrs=0 sa=0 sb=0 sd=0 m=1
XM277_tp3 net17 net8 net35 VDD pfet_05v0 L=0.5u W=0.505u nf=1 ad=2.525e-13 as=2.525e-13 pd=2.01e-06
+ ps=2.01e-06 nrd=0 nrs=0 sa=0 sb=0 sd=0 m=1
XM277_tp10 net35 net7 VDD VDD pfet_05v0 L=0.5u W=0.505u nf=1 ad=2.525e-13 as=2.525e-13 pd=2.01e-06
+ ps=2.01e-06 nrd=0 nrs=0 sa=0 sb=0 sd=0 m=1
XM277_tp5 net7 rst_n VDD VDD pfet_05v0 L=0.5u W=1u nf=1 ad=5e-13 as=5e-13 pd=3e-06 ps=3e-06 nrd=0
+ nrs=0 sa=0 sb=0 sd=0 m=1
XM277_tp4 net7 net17 VDD VDD pfet_05v0 L=0.5u W=1u nf=1 ad=5e-13 as=5e-13 pd=3e-06 ps=3e-06 nrd=0
+ nrs=0 sa=0 sb=0 sd=0 m=1
XM277_tp1 uio_out_3 net7 VDD VDD pfet_05v0 L=0.5u W=1.215u nf=1 ad=6.075e-13 as=6.075e-13
+ pd=3.43e-06 ps=3.43e-06 nrd=0 nrs=0 sa=0 sb=0 sd=0 m=1
**.ends
.GLOBAL VDD
.end
